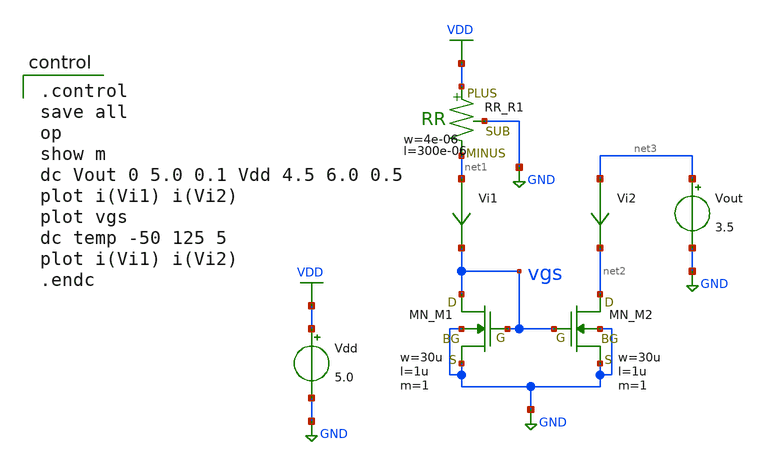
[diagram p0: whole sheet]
** sch_path: OpenSUSI-TR10/current-source/cs-basic.sch
**.subckt cs-basic
Vdd VDD GND 5.0
Vi1 net1 vgs 0
.save i(vi1)
Vi2 net3 net2 0
.save i(vi2)
Vout net3 GND 3.5
XR1 VDD net1 GND F_RR w=4e-06 R=1 l=300e-06 tc1=0 tc2=0
XM1 vgs vgs GND GND NMOS w=30u l=1u as=0 ad=0 ps=0 pd=0 nrd=0 nrs=0 m=1
XM2 net2 vgs GND GND NMOS w=30u l=1u as=0 ad=0 ps=0 pd=0 nrd=0 nrs=0 m=1
**** begin user architecture code

.control
save all
op
show m
dc Vout 0 5.0 0.1 Vdd 4.5 6.0 0.5
plot i(Vi1) i(Vi2)
plot vgs
dc temp -50 125 5
plot i(Vi1) i(Vi2)
.endc

 .include $::LIB/../ip62_models
**** end user architecture code
**.ends
.GLOBAL GND
.GLOBAL VDD
.end
